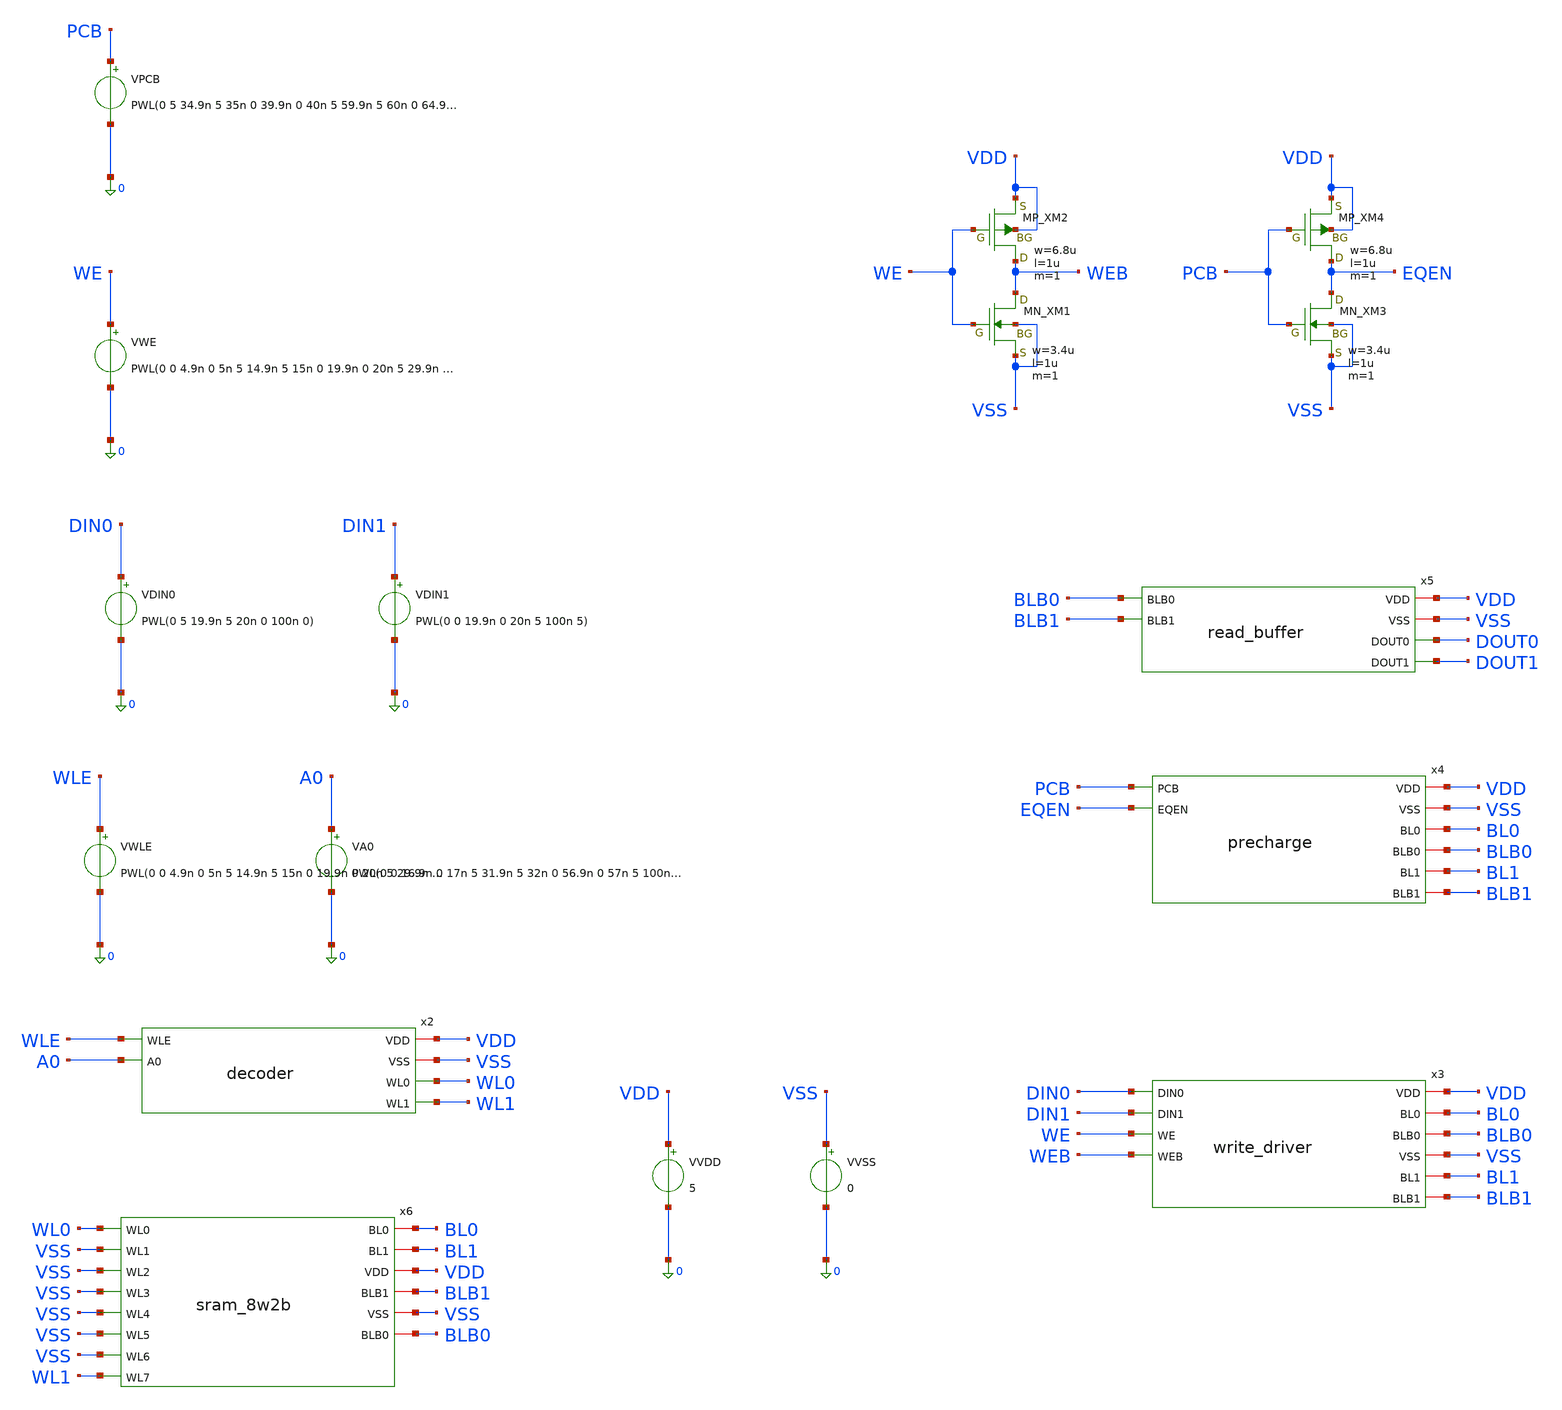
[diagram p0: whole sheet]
** sch_path: array/2word_x_8bit/tb_sram_8w2b.sch
**.subckt tb_sram_8w2b
VVDD VDD 0 5
VDIN0 DIN0 0 PWL(0 5 19.9n 5 20n 0 100n 0)
VVSS VSS 0 0
VWE WE 0 PWL(0 0 4.9n 0 5n 5 14.9n 5 15n 0 19.9n 0 20n 5 29.9n 5 30n 0 100n 0)
VPCB PCB 0 PWL(0 5 34.9n 5 35n 0 39.9n 0 40n 5 59.9n 5 60n 0 64.9n 0 65n 5 100n 5)
x2 VDD VSS WL0 WLE A0 WL1 decoder
VWLE WLE 0 PWL(0 0 4.9n 0 5n 5 14.9n 5 15n 0 19.9n 0 20n 5 29.9n 5 30n 0 44.9n 0 45n 5 54.9n 5 55n 0
+ 69.9n 0 70n 5 79.9n 5 80n 0 100n 0)
VA0 A0 0 PWL(0 0 16.9n 0 17n 5 31.9n 5 32n 0 56.9n 0 57n 5 100n 5)
x3 DIN0 VDD BL0 BLB0 VSS DIN1 BL1 WE BLB1 WEB write_driver
VDIN1 DIN1 0 PWL(0 0 19.9n 0 20n 5 100n 5)
x4 VDD VSS PCB EQEN BL0 BLB0 BL1 BLB1 precharge
x5 VDD VSS BLB0 BLB1 DOUT0 DOUT1 read_buffer
XXM1 WEB WE VSS VSS NMOS w=3.4u l=1u nrd=0 nrs=0 m=1
XXM2 WEB WE VDD VDD PMOS w=6.8u l=1u nrd=0 nrs=0 m=1
XXM3 EQEN PCB VSS VSS NMOS w=3.4u l=1u nrd=0 nrs=0 m=1
XXM4 EQEN PCB VDD VDD PMOS w=6.8u l=1u nrd=0 nrs=0 m=1
x6 WL0 BL0 BL1 VDD BLB1 VSS VSS BLB0 VSS VSS VSS VSS VSS WL1 sram_8w2b
**** begin user architecture code
 .include $::LIB/ip62_models


.tran 10p 100n

.meas tran t_read0 TRIG v(wl0) VAL=2.5 RISE=2 TARG v(dout0) VAL=2.5 RISE=1 TD=40n
.meas tran t_read1 TRIG v(wl1) VAL=2.5 RISE=2 TARG v(dout1) VAL=2.5 RISE=1 TD=65n
.meas tran t_wl0_rise WHEN v(WL0)=2.5 RISE=1
.meas tran t_dout0_rise WHEN v(DOUT0)=2.5 RISE=1
.meas tran td_read0 PARAM='t_dout0_rise-t_wl0_rise'
.meas tran dvbl0_05 FIND par('abs(v(BL0)-v(BLB0))') AT=46.88n
.meas tran dvbl0_10 FIND par('abs(v(BL0)-v(BLB0))') AT=47.38n
.meas tran dvbl1_05 FIND par('abs(v(BL1)-v(BLB1))') AT=46.88n
.meas tran dvbl1_10 FIND par('abs(v(BL1)-v(BLB1))') AT=47.38n
.control
run
plot v(pcb) v(eqen)+6
plot v(wl0) v(wl1)+6 v(dout0)+12 v(dout1)+18
.endc


**** end user architecture code
**.ends
.end
